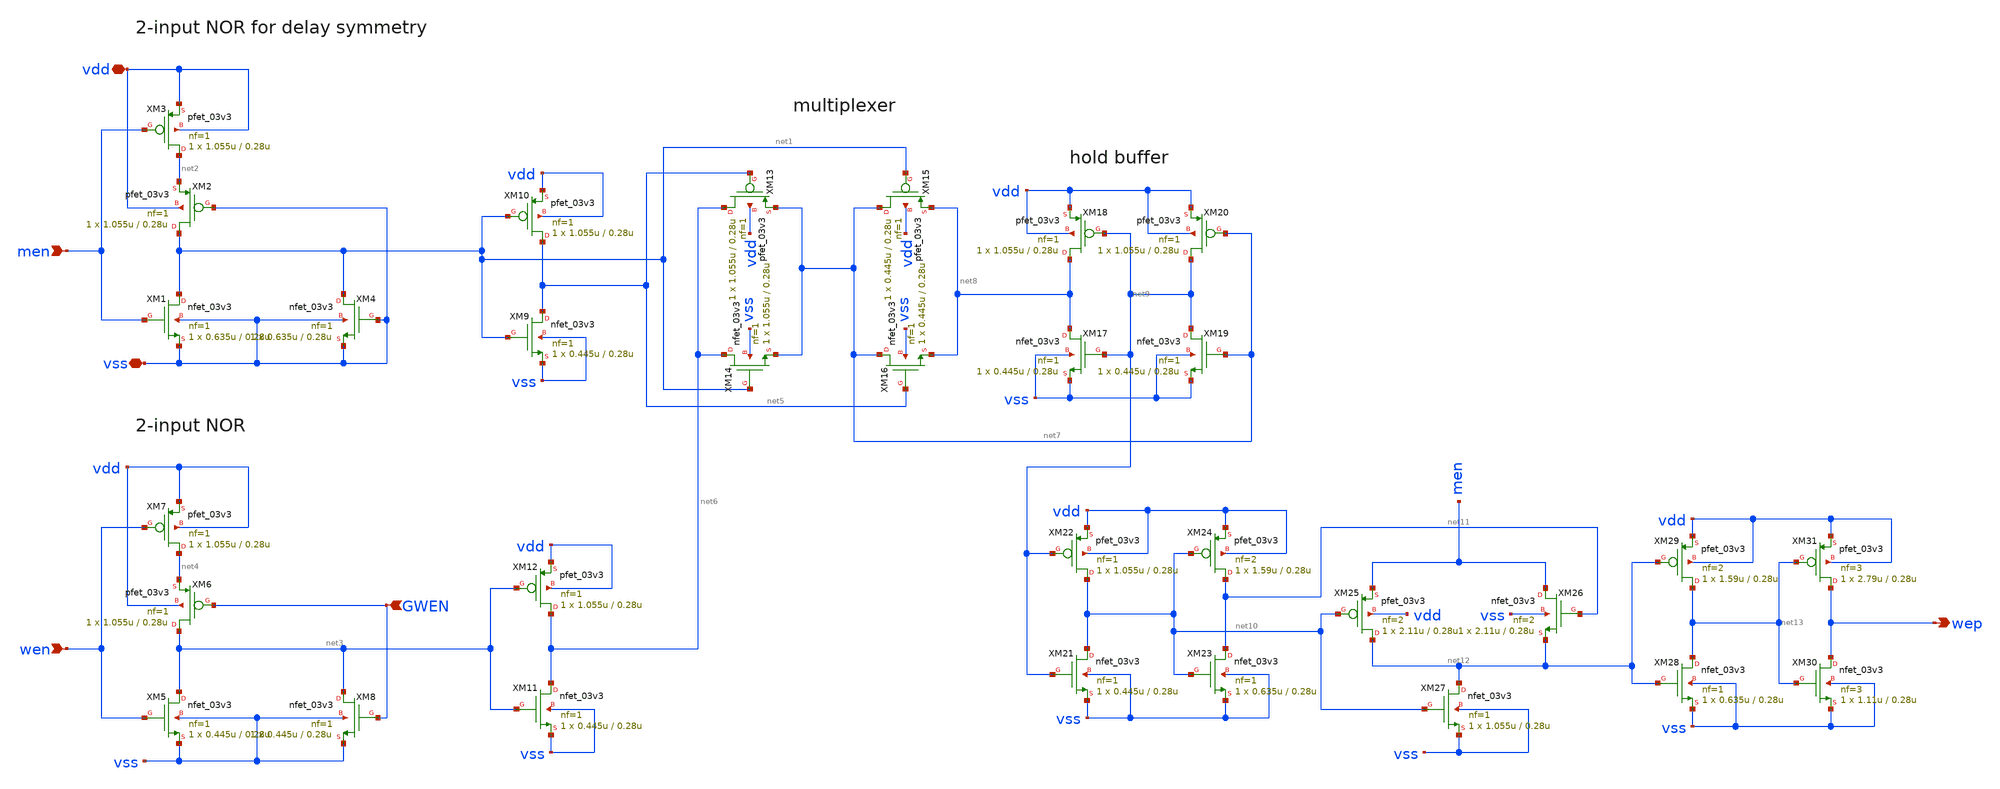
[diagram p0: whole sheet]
** sch_path: cells/gf180mcu_ocd_ip_sram__sram1024x8m8wm1/xschem/wen_wm1_3v1024x8m81.sch
**.subckt wen_wm1_3v1024x8m81 wen men GWEN wep vdd vss
*.ipin wen
*.ipin men
*.ipin GWEN
*.opin wep
*.iopin vdd
*.iopin vss
XM1 net1 men vss vss nfet_03v3 L=0.28u W=0.635u nf=1 ad='int((nf+1)/2) * W/nf * 0.18u' as='int((nf+2)/2) * W/nf * 0.18u'
+ pd='2*int((nf+1)/2) * (W/nf + 0.18u)' ps='2*int((nf+2)/2) * (W/nf + 0.18u)' nrd='0.18u / W' nrs='0.18u / W'
+ sa=0 sb=0 sd=0 m=1
XM2 net1 vss net2 vdd pfet_03v3 L=0.28u W=1.055u nf=1 ad='int((nf+1)/2) * W/nf * 0.18u' as='int((nf+2)/2) * W/nf * 0.18u'
+ pd='2*int((nf+1)/2) * (W/nf + 0.18u)' ps='2*int((nf+2)/2) * (W/nf + 0.18u)' nrd='0.18u / W' nrs='0.18u / W'
+ sa=0 sb=0 sd=0 m=1
XM3 net2 men vdd vdd pfet_03v3 L=0.28u W=1.055u nf=1 ad='int((nf+1)/2) * W/nf * 0.18u' as='int((nf+2)/2) * W/nf * 0.18u'
+ pd='2*int((nf+1)/2) * (W/nf + 0.18u)' ps='2*int((nf+2)/2) * (W/nf + 0.18u)' nrd='0.18u / W' nrs='0.18u / W'
+ sa=0 sb=0 sd=0 m=1
XM4 net1 vss vss vss nfet_03v3 L=0.28u W=0.635u nf=1 ad='int((nf+1)/2) * W/nf * 0.18u' as='int((nf+2)/2) * W/nf * 0.18u'
+ pd='2*int((nf+1)/2) * (W/nf + 0.18u)' ps='2*int((nf+2)/2) * (W/nf + 0.18u)' nrd='0.18u / W' nrs='0.18u / W'
+ sa=0 sb=0 sd=0 m=1
XM5 net3 wen vss vss nfet_03v3 L=0.28u W=0.445u nf=1 ad='int((nf+1)/2) * W/nf * 0.18u' as='int((nf+2)/2) * W/nf * 0.18u'
+ pd='2*int((nf+1)/2) * (W/nf + 0.18u)' ps='2*int((nf+2)/2) * (W/nf + 0.18u)' nrd='0.18u / W' nrs='0.18u / W'
+ sa=0 sb=0 sd=0 m=1
XM6 net3 GWEN net4 vdd pfet_03v3 L=0.28u W=1.055u nf=1 ad='int((nf+1)/2) * W/nf * 0.18u' as='int((nf+2)/2) * W/nf * 0.18u'
+ pd='2*int((nf+1)/2) * (W/nf + 0.18u)' ps='2*int((nf+2)/2) * (W/nf + 0.18u)' nrd='0.18u / W' nrs='0.18u / W'
+ sa=0 sb=0 sd=0 m=1
XM7 net4 wen vdd vdd pfet_03v3 L=0.28u W=1.055u nf=1 ad='int((nf+1)/2) * W/nf * 0.18u' as='int((nf+2)/2) * W/nf * 0.18u'
+ pd='2*int((nf+1)/2) * (W/nf + 0.18u)' ps='2*int((nf+2)/2) * (W/nf + 0.18u)' nrd='0.18u / W' nrs='0.18u / W'
+ sa=0 sb=0 sd=0 m=1
XM8 net3 GWEN vss vss nfet_03v3 L=0.28u W=0.445u nf=1 ad='int((nf+1)/2) * W/nf * 0.18u' as='int((nf+2)/2) * W/nf * 0.18u'
+ pd='2*int((nf+1)/2) * (W/nf + 0.18u)' ps='2*int((nf+2)/2) * (W/nf + 0.18u)' nrd='0.18u / W' nrs='0.18u / W'
+ sa=0 sb=0 sd=0 m=1
XM9 net5 net1 vss vss nfet_03v3 L=0.28u W=0.445u nf=1 ad='int((nf+1)/2) * W/nf * 0.18u' as='int((nf+2)/2) * W/nf * 0.18u'
+ pd='2*int((nf+1)/2) * (W/nf + 0.18u)' ps='2*int((nf+2)/2) * (W/nf + 0.18u)' nrd='0.18u / W' nrs='0.18u / W'
+ sa=0 sb=0 sd=0 m=1
XM10 net5 net1 vdd vdd pfet_03v3 L=0.28u W=1.055u nf=1 ad='int((nf+1)/2) * W/nf * 0.18u' as='int((nf+2)/2) * W/nf * 0.18u'
+ pd='2*int((nf+1)/2) * (W/nf + 0.18u)' ps='2*int((nf+2)/2) * (W/nf + 0.18u)' nrd='0.18u / W' nrs='0.18u / W'
+ sa=0 sb=0 sd=0 m=1
XM11 net6 net3 vss vss nfet_03v3 L=0.28u W=0.445u nf=1 ad='int((nf+1)/2) * W/nf * 0.18u' as='int((nf+2)/2) * W/nf * 0.18u'
+ pd='2*int((nf+1)/2) * (W/nf + 0.18u)' ps='2*int((nf+2)/2) * (W/nf + 0.18u)' nrd='0.18u / W' nrs='0.18u / W'
+ sa=0 sb=0 sd=0 m=1
XM12 net6 net3 vdd vdd pfet_03v3 L=0.28u W=1.055u nf=1 ad='int((nf+1)/2) * W/nf * 0.18u' as='int((nf+2)/2) * W/nf * 0.18u'
+ pd='2*int((nf+1)/2) * (W/nf + 0.18u)' ps='2*int((nf+2)/2) * (W/nf + 0.18u)' nrd='0.18u / W' nrs='0.18u / W'
+ sa=0 sb=0 sd=0 m=1
XM13 net6 net5 net7 vdd pfet_03v3 L=0.28u W=1.055u nf=1 ad='int((nf+1)/2) * W/nf * 0.18u' as='int((nf+2)/2) * W/nf * 0.18u'
+ pd='2*int((nf+1)/2) * (W/nf + 0.18u)' ps='2*int((nf+2)/2) * (W/nf + 0.18u)' nrd='0.18u / W' nrs='0.18u / W'
+ sa=0 sb=0 sd=0 m=1
XM14 net6 net1 net7 vss nfet_03v3 L=0.28u W=1.055u nf=1 ad='int((nf+1)/2) * W/nf * 0.18u' as='int((nf+2)/2) * W/nf * 0.18u'
+ pd='2*int((nf+1)/2) * (W/nf + 0.18u)' ps='2*int((nf+2)/2) * (W/nf + 0.18u)' nrd='0.18u / W' nrs='0.18u / W'
+ sa=0 sb=0 sd=0 m=1
XM15 net7 net1 net8 vdd pfet_03v3 L=0.28u W=0.445u nf=1 ad='int((nf+1)/2) * W/nf * 0.18u' as='int((nf+2)/2) * W/nf * 0.18u'
+ pd='2*int((nf+1)/2) * (W/nf + 0.18u)' ps='2*int((nf+2)/2) * (W/nf + 0.18u)' nrd='0.18u / W' nrs='0.18u / W'
+ sa=0 sb=0 sd=0 m=1
XM16 net7 net5 net8 vss nfet_03v3 L=0.28u W=0.445u nf=1 ad='int((nf+1)/2) * W/nf * 0.18u' as='int((nf+2)/2) * W/nf * 0.18u'
+ pd='2*int((nf+1)/2) * (W/nf + 0.18u)' ps='2*int((nf+2)/2) * (W/nf + 0.18u)' nrd='0.18u / W' nrs='0.18u / W'
+ sa=0 sb=0 sd=0 m=1
XM17 net8 net9 vss vss nfet_03v3 L=0.28u W=0.445u nf=1 ad='int((nf+1)/2) * W/nf * 0.18u' as='int((nf+2)/2) * W/nf * 0.18u'
+ pd='2*int((nf+1)/2) * (W/nf + 0.18u)' ps='2*int((nf+2)/2) * (W/nf + 0.18u)' nrd='0.18u / W' nrs='0.18u / W'
+ sa=0 sb=0 sd=0 m=1
XM18 net8 net9 vdd vdd pfet_03v3 L=0.28u W=1.055u nf=1 ad='int((nf+1)/2) * W/nf * 0.18u' as='int((nf+2)/2) * W/nf * 0.18u'
+ pd='2*int((nf+1)/2) * (W/nf + 0.18u)' ps='2*int((nf+2)/2) * (W/nf + 0.18u)' nrd='0.18u / W' nrs='0.18u / W'
+ sa=0 sb=0 sd=0 m=1
XM19 net9 net7 vss vss nfet_03v3 L=0.28u W=0.445u nf=1 ad='int((nf+1)/2) * W/nf * 0.18u' as='int((nf+2)/2) * W/nf * 0.18u'
+ pd='2*int((nf+1)/2) * (W/nf + 0.18u)' ps='2*int((nf+2)/2) * (W/nf + 0.18u)' nrd='0.18u / W' nrs='0.18u / W'
+ sa=0 sb=0 sd=0 m=1
XM20 net9 net7 vdd vdd pfet_03v3 L=0.28u W=1.055u nf=1 ad='int((nf+1)/2) * W/nf * 0.18u' as='int((nf+2)/2) * W/nf * 0.18u'
+ pd='2*int((nf+1)/2) * (W/nf + 0.18u)' ps='2*int((nf+2)/2) * (W/nf + 0.18u)' nrd='0.18u / W' nrs='0.18u / W'
+ sa=0 sb=0 sd=0 m=1
XM21 net10 net9 vss vss nfet_03v3 L=0.28u W=0.445u nf=1 ad='int((nf+1)/2) * W/nf * 0.18u' as='int((nf+2)/2) * W/nf * 0.18u'
+ pd='2*int((nf+1)/2) * (W/nf + 0.18u)' ps='2*int((nf+2)/2) * (W/nf + 0.18u)' nrd='0.18u / W' nrs='0.18u / W'
+ sa=0 sb=0 sd=0 m=1
XM22 net10 net9 vdd vdd pfet_03v3 L=0.28u W=1.055u nf=1 ad='int((nf+1)/2) * W/nf * 0.18u' as='int((nf+2)/2) * W/nf * 0.18u'
+ pd='2*int((nf+1)/2) * (W/nf + 0.18u)' ps='2*int((nf+2)/2) * (W/nf + 0.18u)' nrd='0.18u / W' nrs='0.18u / W'
+ sa=0 sb=0 sd=0 m=1
XM23 net11 net10 vss vss nfet_03v3 L=0.28u W=0.635u nf=1 ad='int((nf+1)/2) * W/nf * 0.18u' as='int((nf+2)/2) * W/nf * 0.18u'
+ pd='2*int((nf+1)/2) * (W/nf + 0.18u)' ps='2*int((nf+2)/2) * (W/nf + 0.18u)' nrd='0.18u / W' nrs='0.18u / W'
+ sa=0 sb=0 sd=0 m=1
XM24 net11 net10 vdd vdd pfet_03v3 L=0.28u W=1.59u nf=2 ad='int((nf+1)/2) * W/nf * 0.18u' as='int((nf+2)/2) * W/nf * 0.18u'
+ pd='2*int((nf+1)/2) * (W/nf + 0.18u)' ps='2*int((nf+2)/2) * (W/nf + 0.18u)' nrd='0.18u / W' nrs='0.18u / W'
+ sa=0 sb=0 sd=0 m=1
XM25 net12 net10 men vdd pfet_03v3 L=0.28u W=2.11u nf=2 ad='int((nf+1)/2) * W/nf * 0.18u' as='int((nf+2)/2) * W/nf * 0.18u'
+ pd='2*int((nf+1)/2) * (W/nf + 0.18u)' ps='2*int((nf+2)/2) * (W/nf + 0.18u)' nrd='0.18u / W' nrs='0.18u / W'
+ sa=0 sb=0 sd=0 m=1
XM26 men net11 net12 vss nfet_03v3 L=0.28u W=2.11u nf=2 ad='int((nf+1)/2) * W/nf * 0.18u' as='int((nf+2)/2) * W/nf * 0.18u'
+ pd='2*int((nf+1)/2) * (W/nf + 0.18u)' ps='2*int((nf+2)/2) * (W/nf + 0.18u)' nrd='0.18u / W' nrs='0.18u / W'
+ sa=0 sb=0 sd=0 m=1
XM27 net12 net10 vss vss nfet_03v3 L=0.28u W=1.055u nf=1 ad='int((nf+1)/2) * W/nf * 0.18u' as='int((nf+2)/2) * W/nf * 0.18u'
+ pd='2*int((nf+1)/2) * (W/nf + 0.18u)' ps='2*int((nf+2)/2) * (W/nf + 0.18u)' nrd='0.18u / W' nrs='0.18u / W'
+ sa=0 sb=0 sd=0 m=1
XM28 net13 net12 vss vss nfet_03v3 L=0.28u W=0.635u nf=1 ad='int((nf+1)/2) * W/nf * 0.18u' as='int((nf+2)/2) * W/nf * 0.18u'
+ pd='2*int((nf+1)/2) * (W/nf + 0.18u)' ps='2*int((nf+2)/2) * (W/nf + 0.18u)' nrd='0.18u / W' nrs='0.18u / W'
+ sa=0 sb=0 sd=0 m=1
XM29 net13 net12 vdd vdd pfet_03v3 L=0.28u W=1.59u nf=2 ad='int((nf+1)/2) * W/nf * 0.18u' as='int((nf+2)/2) * W/nf * 0.18u'
+ pd='2*int((nf+1)/2) * (W/nf + 0.18u)' ps='2*int((nf+2)/2) * (W/nf + 0.18u)' nrd='0.18u / W' nrs='0.18u / W'
+ sa=0 sb=0 sd=0 m=1
XM30 wep net13 vss vss nfet_03v3 L=0.28u W=1.11u nf=3 ad='int((nf+1)/2) * W/nf * 0.18u' as='int((nf+2)/2) * W/nf * 0.18u'
+ pd='2*int((nf+1)/2) * (W/nf + 0.18u)' ps='2*int((nf+2)/2) * (W/nf + 0.18u)' nrd='0.18u / W' nrs='0.18u / W'
+ sa=0 sb=0 sd=0 m=1
XM31 wep net13 vdd vdd pfet_03v3 L=0.28u W=2.79u nf=3 ad='int((nf+1)/2) * W/nf * 0.18u' as='int((nf+2)/2) * W/nf * 0.18u'
+ pd='2*int((nf+1)/2) * (W/nf + 0.18u)' ps='2*int((nf+2)/2) * (W/nf + 0.18u)' nrd='0.18u / W' nrs='0.18u / W'
+ sa=0 sb=0 sd=0 m=1
**.ends
.end
